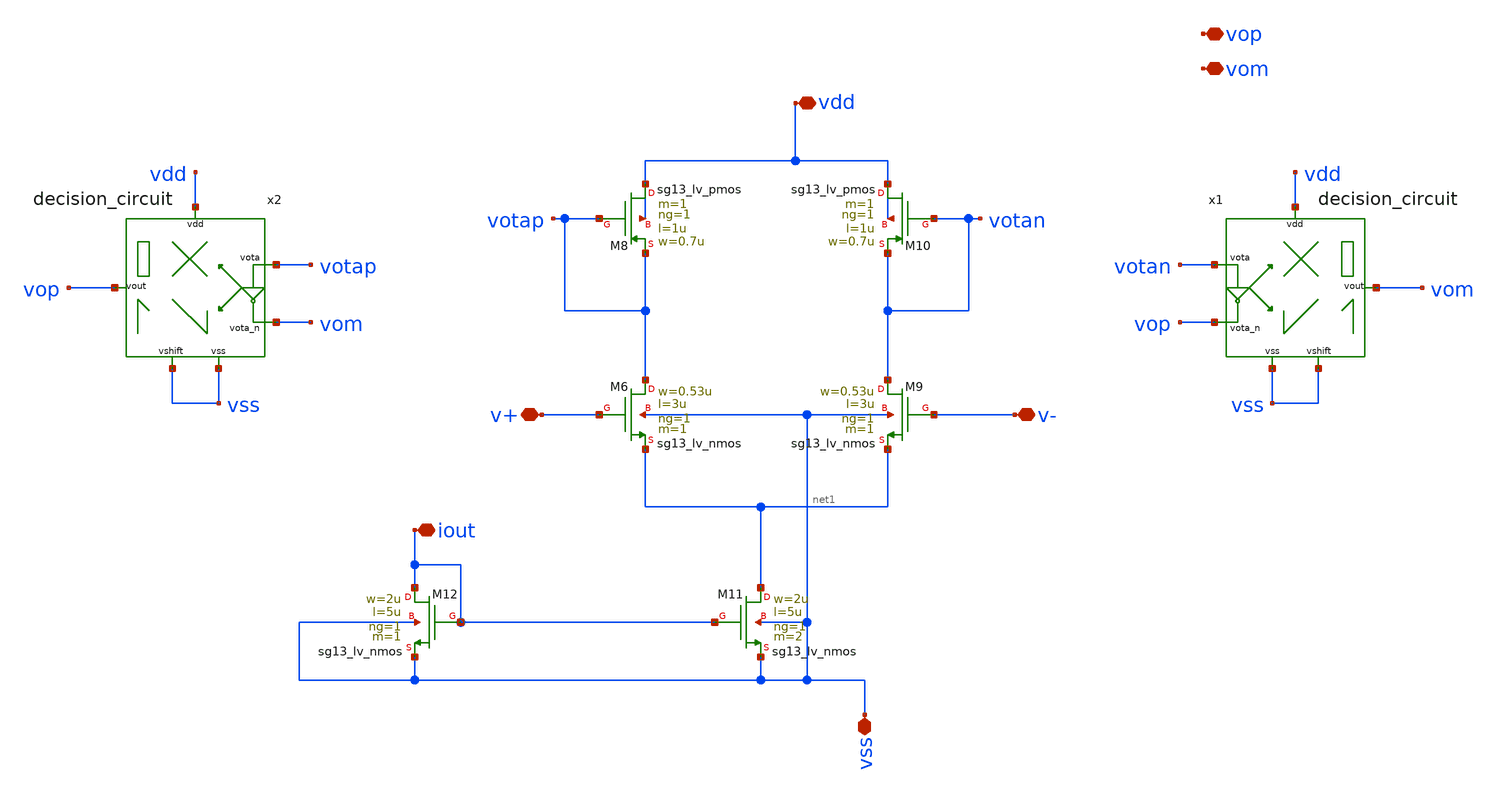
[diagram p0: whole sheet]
** sch_path: schematic/xschem/comparator_stg1/comparator_stg1.sch
**.subckt comparator_stg1 vdd vss v- v+ vom iout vop
*.iopin vdd
*.iopin vss
*.iopin v-
*.iopin v+
*.iopin vom
*.iopin iout
*.iopin vop
XM6 votap v+ net1 vss sg13_lv_nmos w=0.53u l=3u ng=1 m=1 mm_ok=1
XM8 vdd votap votap vdd sg13_lv_pmos w=0.7u l=1u ng=1 m=1 mm_ok=1
XM9 votan v- net1 vss sg13_lv_nmos w=0.53u l=3u ng=1 m=1 mm_ok=1
XM10 vdd votan votan vdd sg13_lv_pmos w=0.7u l=1u ng=1 m=1 mm_ok=1
XM11 net1 iout vss vss sg13_lv_nmos w=2u l=5u ng=1 m=2 mm_ok=1
XM12 iout iout vss vss sg13_lv_nmos w=2u l=5u ng=1 m=1 mm_ok=1
x1 vdd votan vom vop vss vss decision_circuit
x2 vdd votap vop vom vss vss decision_circuit
**.ends

* expanding   symbol:  decision_circuit/decision_circuit.sym # of pins=6
** sym_path: schematic/xschem/decision_circuit/decision_circuit.sym
** sch_path: schematic/xschem/decision_circuit/decision_circuit.sch
.subckt decision_circuit vdd vota vout vota_n vss shift
*.iopin vota
*.iopin shift
*.iopin vota_n
*.iopin vdd
*.iopin vss
*.iopin vout
XM1 vout vota vdd vdd sg13_lv_pmos w=0.7u l=1u ng=1 m=1 mm_ok=1
XM2 vout vout shift vss sg13_lv_nmos w=0.26u l=10u ng=1 m=2 mm_ok=1
XM3 vout vota_n shift vss sg13_lv_nmos w=0.26u l=10u ng=1 m=2 mm_ok=1
XM4 vss vss vout vss sg13_lv_nmos w=0.26u l=0.5u ng=1 m=4 mm_ok=1
XM5 vdd vdd vout vdd sg13_lv_pmos w=0.35u l=0.5u ng=1 m=2 mm_ok=1
.ends

.end
